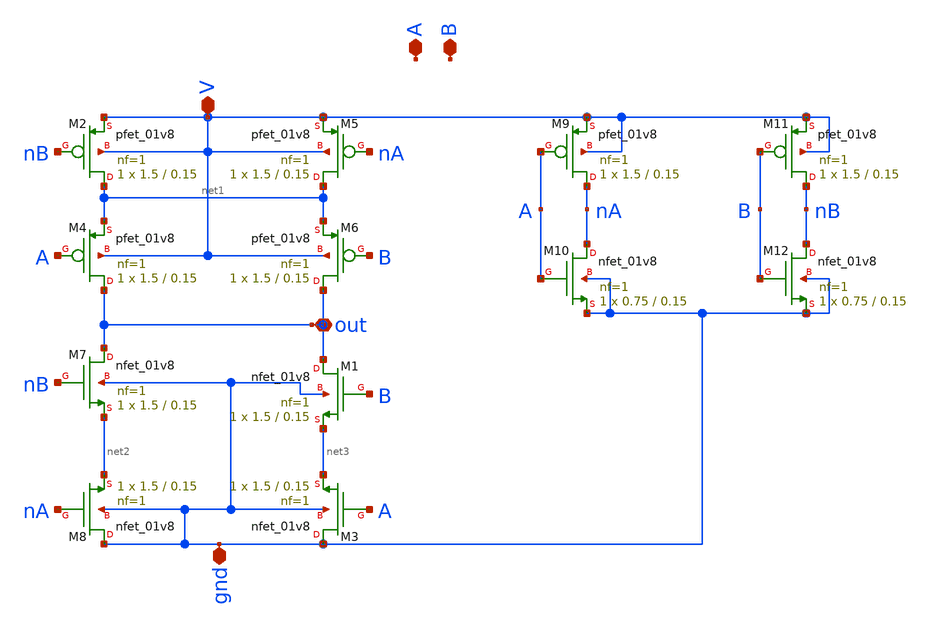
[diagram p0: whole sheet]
** sch_path: EAMTA/xschem/counter4b/symbol/xor_gate.sch
**.subckt xor_gate A out gnd V B
*.iopin A
*.iopin out
*.iopin gnd
*.iopin V
*.iopin B
XM1 out B net3 gnd sky130_fd_pr__nfet_01v8 L=0.15 W=1.5 nf=1 ad='int((nf+1)/2) * W/nf * 0.29' as='int((nf+2)/2) * W/nf * 0.29'
+ pd='2*int((nf+1)/2) * (W/nf + 0.29)' ps='2*int((nf+2)/2) * (W/nf + 0.29)' nrd='0.29 / W' nrs='0.29 / W'
+ sa=0 sb=0 sd=0 mult=1 m=1
XM2 net1 nB V V sky130_fd_pr__pfet_01v8 L=0.15 W=1.5 nf=1 ad='int((nf+1)/2) * W/nf * 0.29' as='int((nf+2)/2) * W/nf * 0.29'
+ pd='2*int((nf+1)/2) * (W/nf + 0.29)' ps='2*int((nf+2)/2) * (W/nf + 0.29)' nrd='0.29 / W' nrs='0.29 / W'
+ sa=0 sb=0 sd=0 mult=1 m=1
XM3 gnd A net3 gnd sky130_fd_pr__nfet_01v8 L=0.15 W=1.5 nf=1 ad='int((nf+1)/2) * W/nf * 0.29' as='int((nf+2)/2) * W/nf * 0.29'
+ pd='2*int((nf+1)/2) * (W/nf + 0.29)' ps='2*int((nf+2)/2) * (W/nf + 0.29)' nrd='0.29 / W' nrs='0.29 / W'
+ sa=0 sb=0 sd=0 mult=1 m=1
XM4 out A net1 V sky130_fd_pr__pfet_01v8 L=0.15 W=1.5 nf=1 ad='int((nf+1)/2) * W/nf * 0.29' as='int((nf+2)/2) * W/nf * 0.29'
+ pd='2*int((nf+1)/2) * (W/nf + 0.29)' ps='2*int((nf+2)/2) * (W/nf + 0.29)' nrd='0.29 / W' nrs='0.29 / W'
+ sa=0 sb=0 sd=0 mult=1 m=1
XM5 net1 nA V V sky130_fd_pr__pfet_01v8 L=0.15 W=1.5 nf=1 ad='int((nf+1)/2) * W/nf * 0.29' as='int((nf+2)/2) * W/nf * 0.29'
+ pd='2*int((nf+1)/2) * (W/nf + 0.29)' ps='2*int((nf+2)/2) * (W/nf + 0.29)' nrd='0.29 / W' nrs='0.29 / W'
+ sa=0 sb=0 sd=0 mult=1 m=1
XM6 out B net1 V sky130_fd_pr__pfet_01v8 L=0.15 W=1.5 nf=1 ad='int((nf+1)/2) * W/nf * 0.29' as='int((nf+2)/2) * W/nf * 0.29'
+ pd='2*int((nf+1)/2) * (W/nf + 0.29)' ps='2*int((nf+2)/2) * (W/nf + 0.29)' nrd='0.29 / W' nrs='0.29 / W'
+ sa=0 sb=0 sd=0 mult=1 m=1
XM7 out nB net2 gnd sky130_fd_pr__nfet_01v8 L=0.15 W=1.5 nf=1 ad='int((nf+1)/2) * W/nf * 0.29' as='int((nf+2)/2) * W/nf * 0.29'
+ pd='2*int((nf+1)/2) * (W/nf + 0.29)' ps='2*int((nf+2)/2) * (W/nf + 0.29)' nrd='0.29 / W' nrs='0.29 / W'
+ sa=0 sb=0 sd=0 mult=1 m=1
XM8 gnd nA net2 gnd sky130_fd_pr__nfet_01v8 L=0.15 W=1.5 nf=1 ad='int((nf+1)/2) * W/nf * 0.29' as='int((nf+2)/2) * W/nf * 0.29'
+ pd='2*int((nf+1)/2) * (W/nf + 0.29)' ps='2*int((nf+2)/2) * (W/nf + 0.29)' nrd='0.29 / W' nrs='0.29 / W'
+ sa=0 sb=0 sd=0 mult=1 m=1
XM9 nA A V V sky130_fd_pr__pfet_01v8 L=0.15 W=1.5 nf=1 ad='int((nf+1)/2) * W/nf * 0.29' as='int((nf+2)/2) * W/nf * 0.29'
+ pd='2*int((nf+1)/2) * (W/nf + 0.29)' ps='2*int((nf+2)/2) * (W/nf + 0.29)' nrd='0.29 / W' nrs='0.29 / W'
+ sa=0 sb=0 sd=0 mult=1 m=1
XM10 nA A gnd gnd sky130_fd_pr__nfet_01v8 L=0.15 W=0.75 nf=1 ad='int((nf+1)/2) * W/nf * 0.29' as='int((nf+2)/2) * W/nf * 0.29'
+ pd='2*int((nf+1)/2) * (W/nf + 0.29)' ps='2*int((nf+2)/2) * (W/nf + 0.29)' nrd='0.29 / W' nrs='0.29 / W'
+ sa=0 sb=0 sd=0 mult=1 m=1
XM11 nB B V V sky130_fd_pr__pfet_01v8 L=0.15 W=1.5 nf=1 ad='int((nf+1)/2) * W/nf * 0.29' as='int((nf+2)/2) * W/nf * 0.29'
+ pd='2*int((nf+1)/2) * (W/nf + 0.29)' ps='2*int((nf+2)/2) * (W/nf + 0.29)' nrd='0.29 / W' nrs='0.29 / W'
+ sa=0 sb=0 sd=0 mult=1 m=1
XM12 nB B gnd gnd sky130_fd_pr__nfet_01v8 L=0.15 W=0.75 nf=1 ad='int((nf+1)/2) * W/nf * 0.29' as='int((nf+2)/2) * W/nf * 0.29'
+ pd='2*int((nf+1)/2) * (W/nf + 0.29)' ps='2*int((nf+2)/2) * (W/nf + 0.29)' nrd='0.29 / W' nrs='0.29 / W'
+ sa=0 sb=0 sd=0 mult=1 m=1
**.ends
.end
